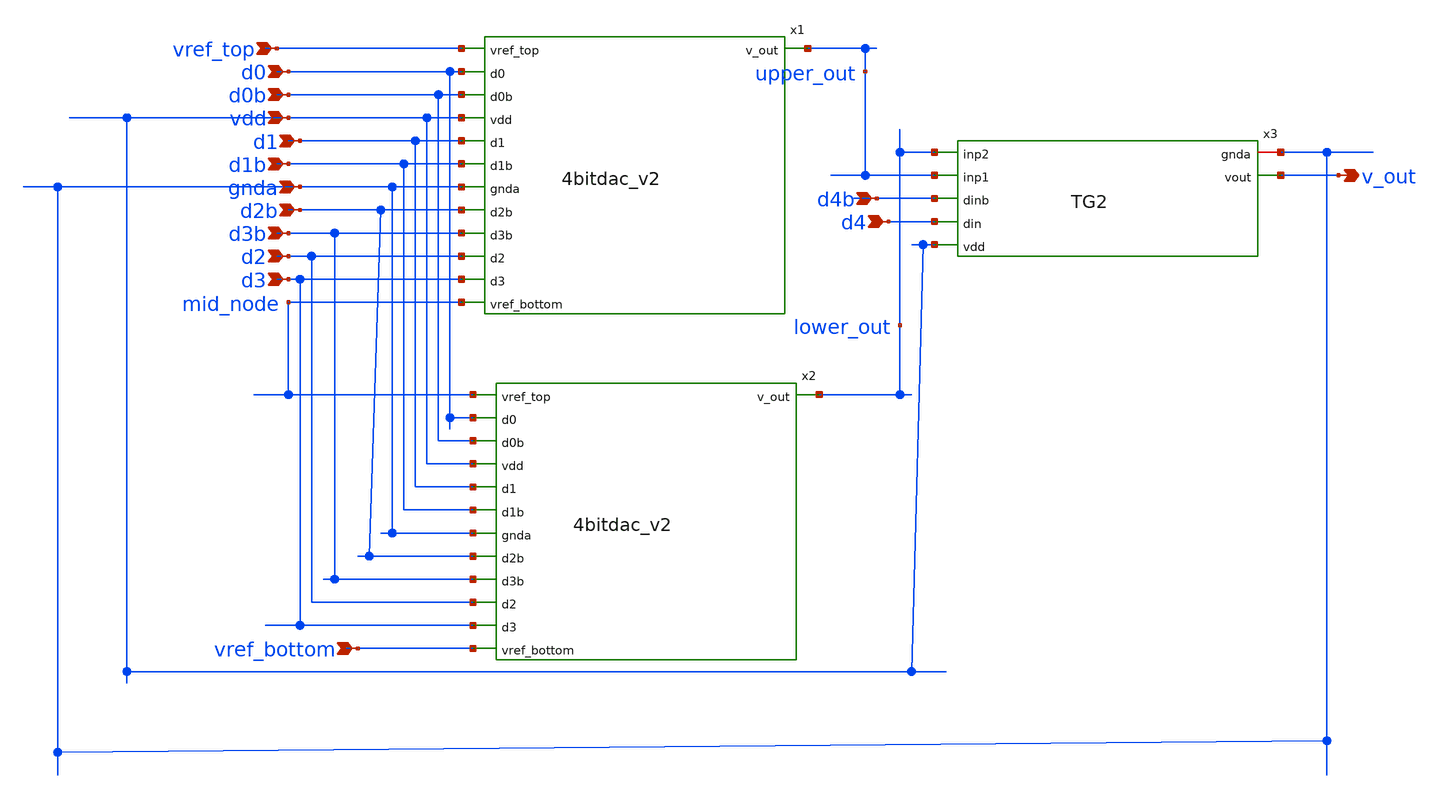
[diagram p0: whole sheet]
** sch_path: prelayout/5bitdac_v2.sch
**.subckt 5bitdac_v2 vref_top d0 vdd d1b d0b d1 gnda d2b d3b d2 d3 d4b d4 v_out vref_bottom
*.ipin vref_top
*.ipin d0
*.ipin vdd
*.ipin d1b
*.ipin d0b
*.ipin d1
*.ipin gnda
*.ipin d2b
*.ipin d3b
*.ipin d2
*.ipin d3
*.ipin d4b
*.ipin d4
*.opin v_out
*.ipin vref_bottom
Xx3 gnda v_out lower_out upper_out d4b d4 vdd TG2
x1 vref_top d0 d0b vdd d1 d1b gnda upper_out d2b d3b d2 d3 mid_node 4bitdac_v2
x2 mid_node d0 d0b vdd d1 d1b gnda lower_out d2b d3b d2 d3 vref_bottom 4bitdac_v2
**.ends
.end
